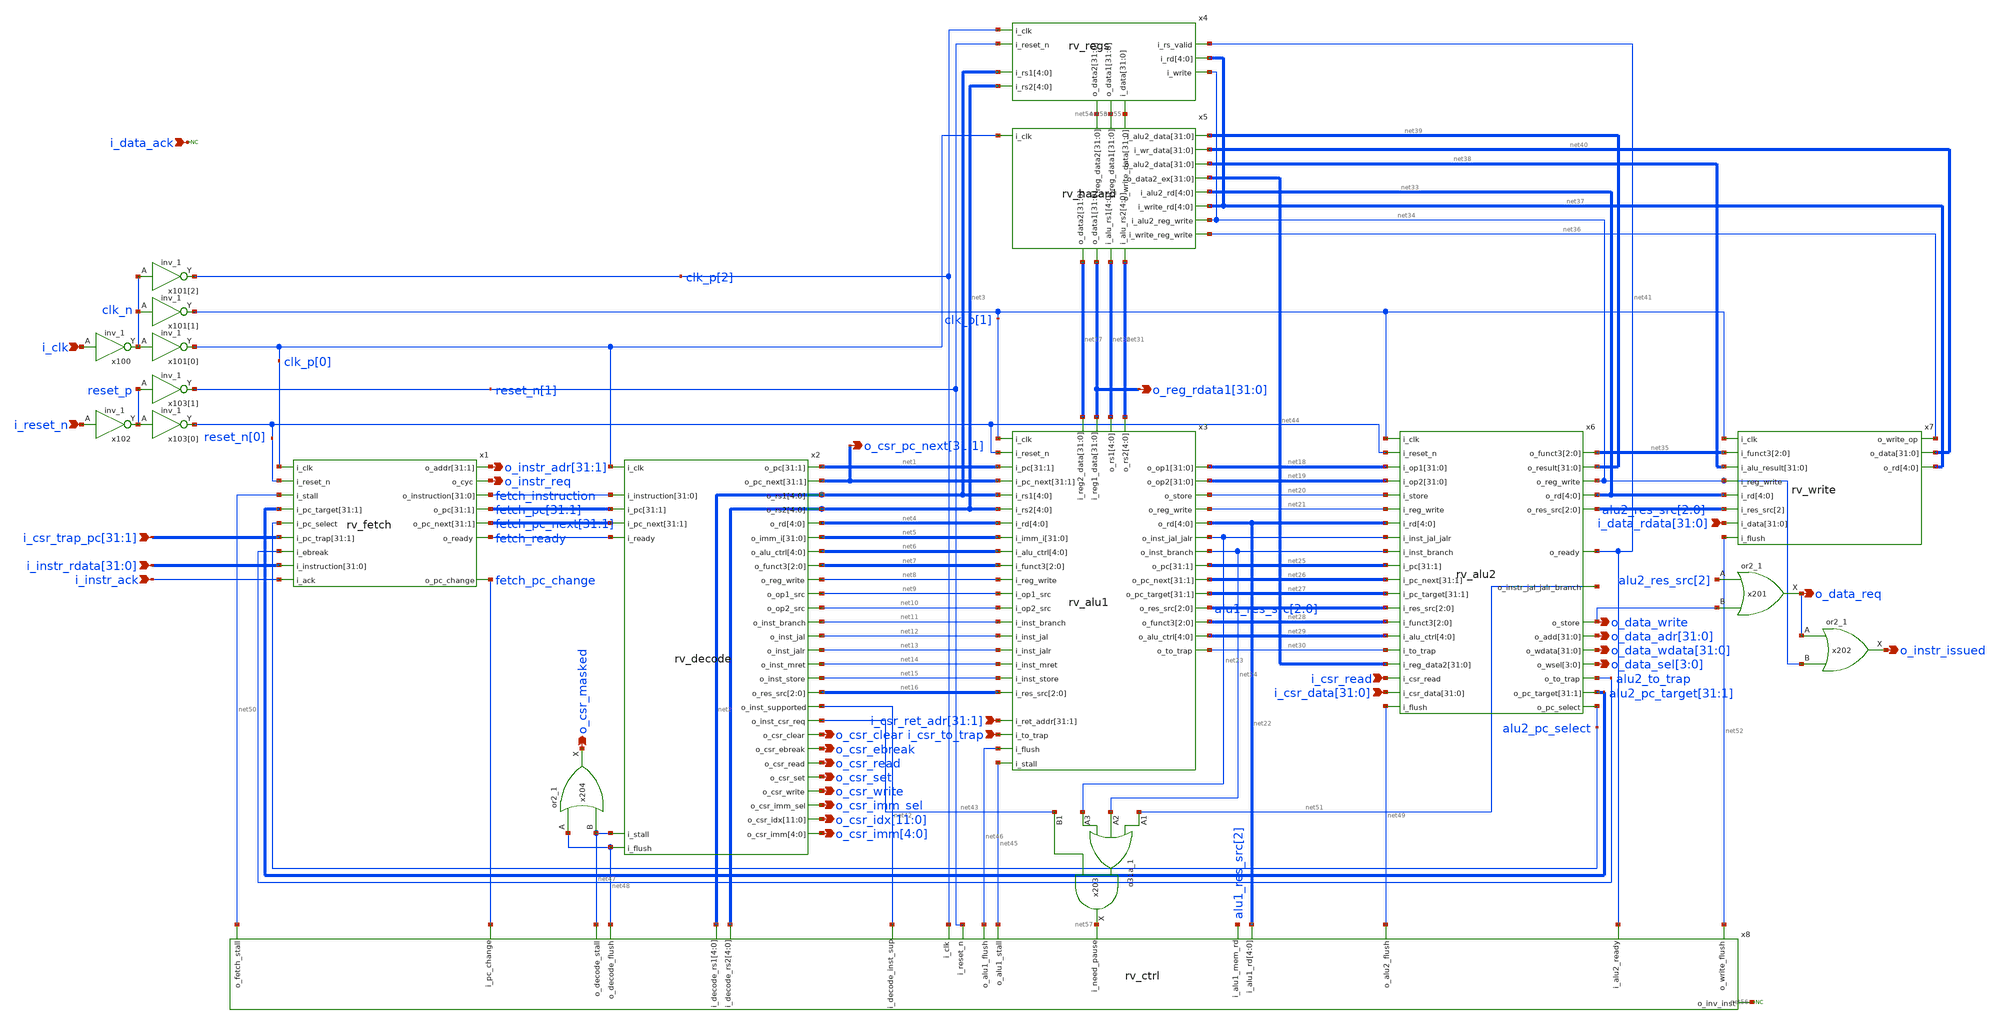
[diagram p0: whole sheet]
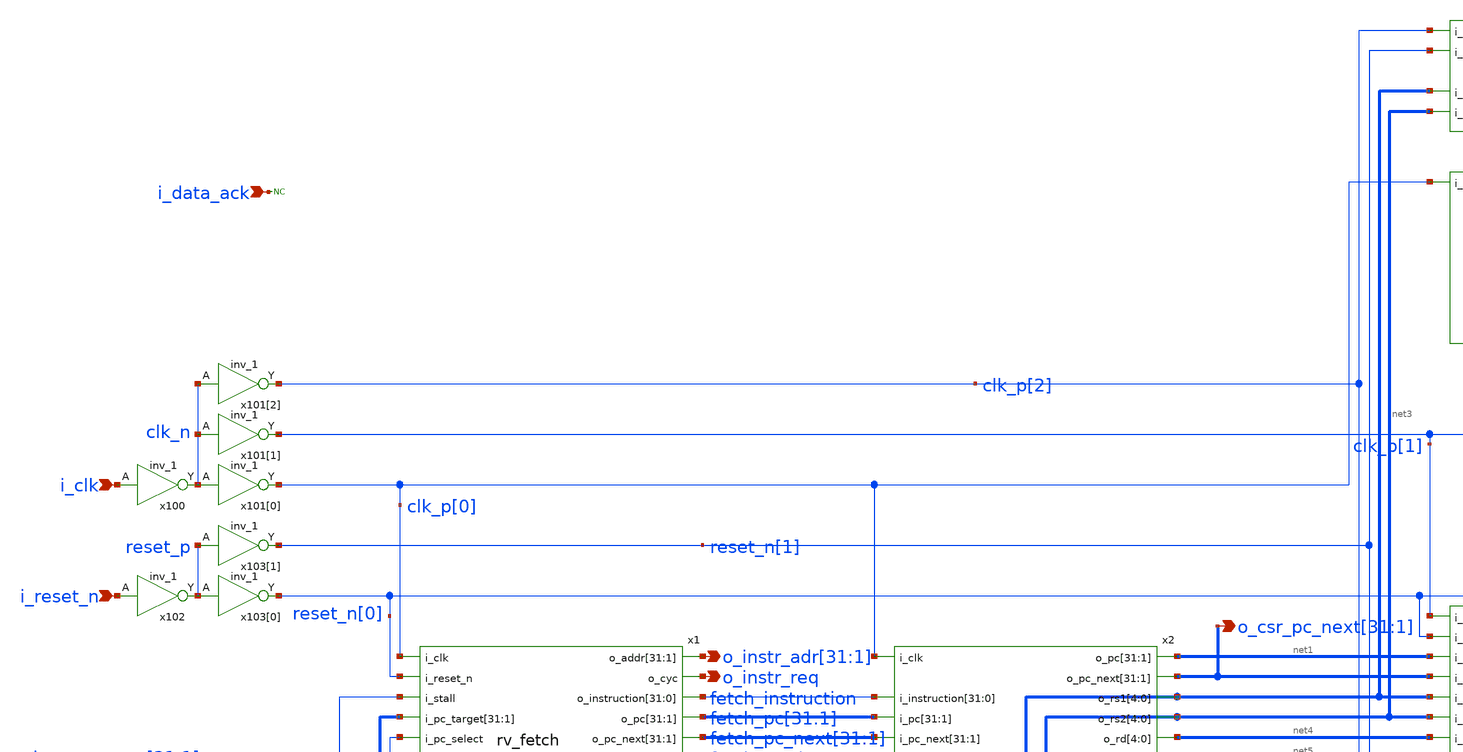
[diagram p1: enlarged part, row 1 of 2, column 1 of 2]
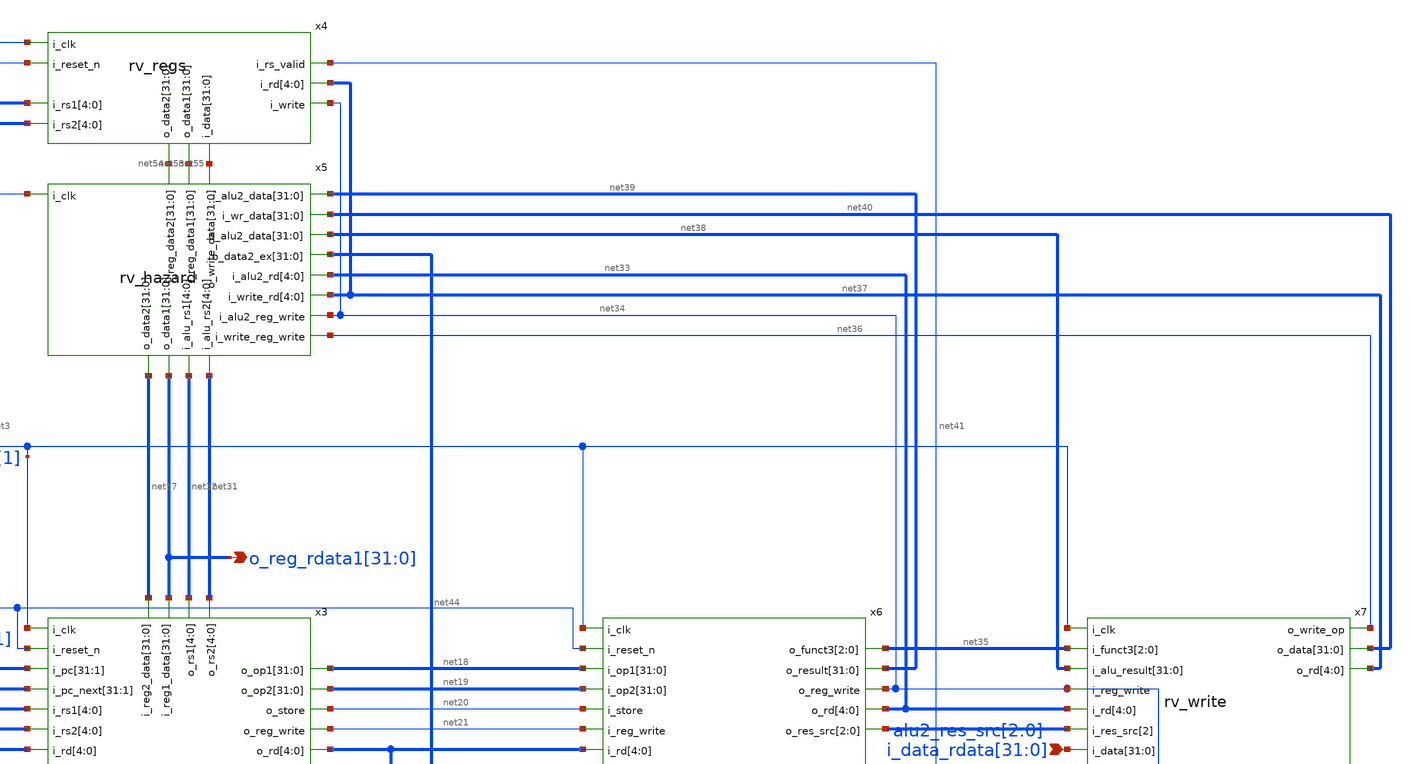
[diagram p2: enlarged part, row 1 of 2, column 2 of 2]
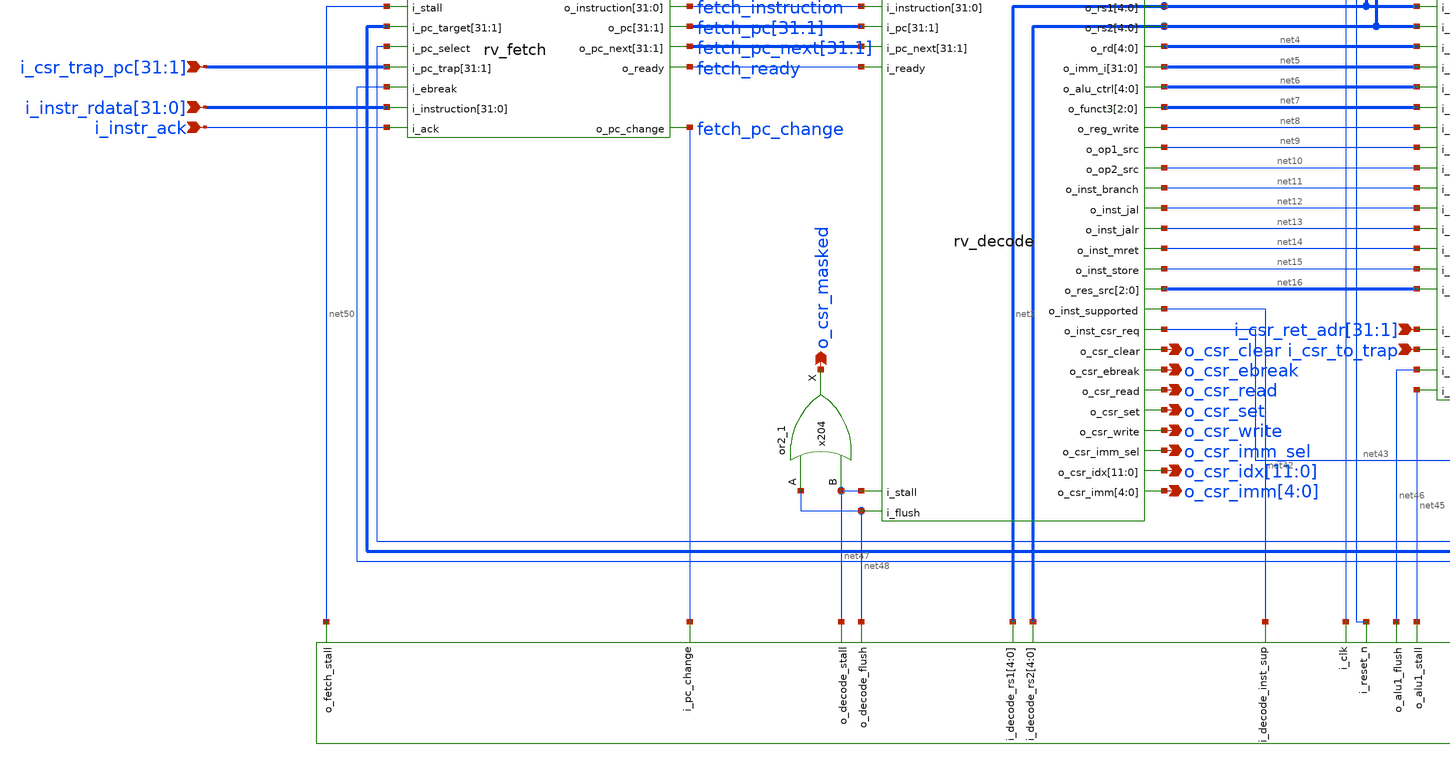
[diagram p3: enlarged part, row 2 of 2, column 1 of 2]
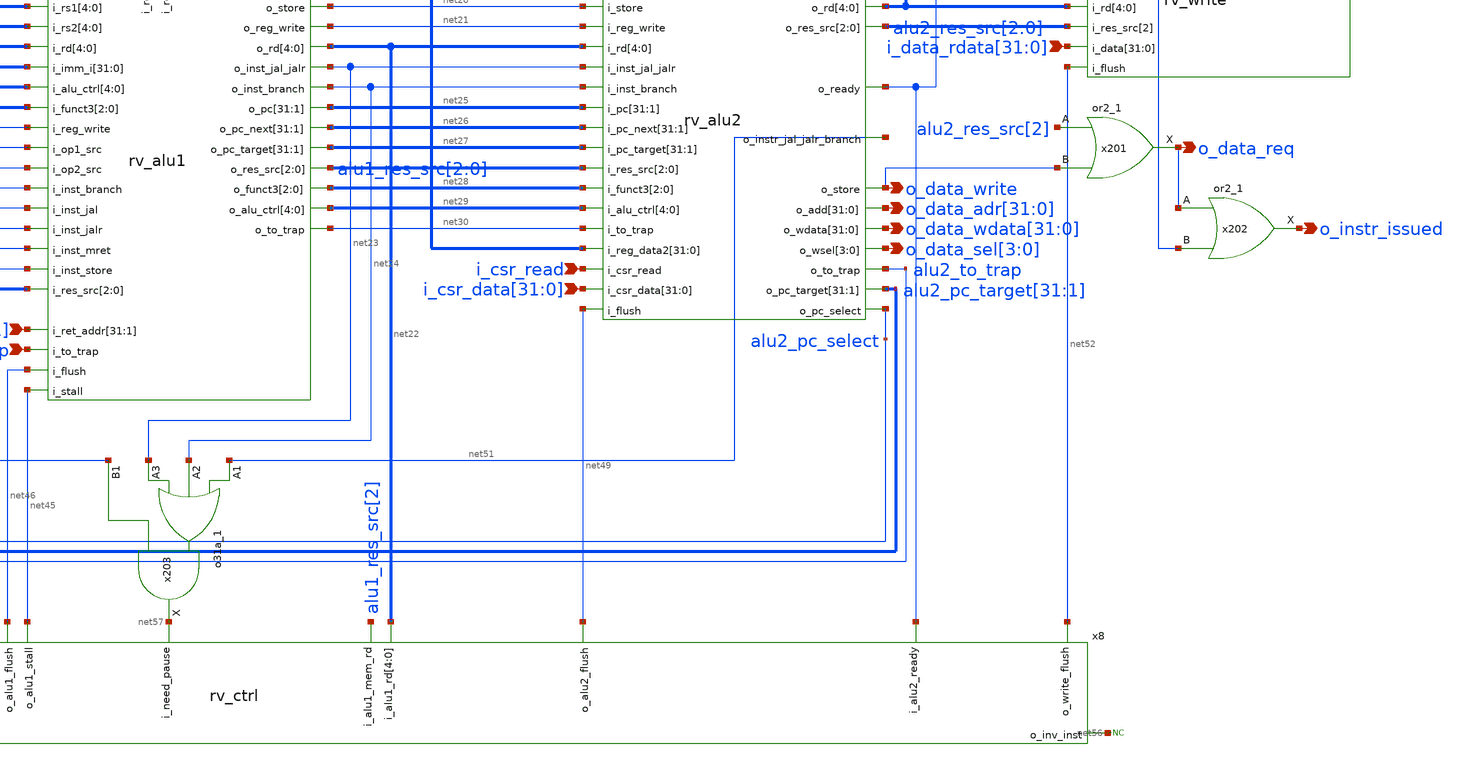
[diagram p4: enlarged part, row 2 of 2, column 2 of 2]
** sch_path: blocks/rv_core/rv_core.sch
**.subckt rv_core i_clk i_reset_n i_csr_read o_csr_clear o_data_req
*+ o_data_wdata[31],o_data_wdata[30],o_data_wdata[29],o_data_wdata[28],o_data_wdata[27],o_data_wdata[26],o_data_wdata[25],o_data_wdata[24],o_data_wdata[23],o_data_wdata[22],o_data_wdata[21],o_data_wdata[20],o_data_wdata[19],o_data_wdata[18],o_data_wdata[17],o_data_wdata[16],o_data_wdata[15],o_data_wdata[14],o_data_wdata[13],o_data_wdata[12],o_data_wdata[11],o_data_wdata[10],o_data_wdata[9],o_data_wdata[8],o_data_wdata[7],o_data_wdata[6],o_data_wdata[5],o_data_wdata[4],o_data_wdata[3],o_data_wdata[2],o_data_wdata[1],o_data_wdata[0] o_instr_issued
*+ o_data_adr[31],o_data_adr[30],o_data_adr[29],o_data_adr[28],o_data_adr[27],o_data_adr[26],o_data_adr[25],o_data_adr[24],o_data_adr[23],o_data_adr[22],o_data_adr[21],o_data_adr[20],o_data_adr[19],o_data_adr[18],o_data_adr[17],o_data_adr[16],o_data_adr[15],o_data_adr[14],o_data_adr[13],o_data_adr[12],o_data_adr[11],o_data_adr[10],o_data_adr[9],o_data_adr[8],o_data_adr[7],o_data_adr[6],o_data_adr[5],o_data_adr[4],o_data_adr[3],o_data_adr[2],o_data_adr[1],o_data_adr[0] o_data_sel[3],o_data_sel[2],o_data_sel[1],o_data_sel[0]
*+ i_csr_data[31],i_csr_data[30],i_csr_data[29],i_csr_data[28],i_csr_data[27],i_csr_data[26],i_csr_data[25],i_csr_data[24],i_csr_data[23],i_csr_data[22],i_csr_data[21],i_csr_data[20],i_csr_data[19],i_csr_data[18],i_csr_data[17],i_csr_data[16],i_csr_data[15],i_csr_data[14],i_csr_data[13],i_csr_data[12],i_csr_data[11],i_csr_data[10],i_csr_data[9],i_csr_data[8],i_csr_data[7],i_csr_data[6],i_csr_data[5],i_csr_data[4],i_csr_data[3],i_csr_data[2],i_csr_data[1],i_csr_data[0] i_csr_to_trap o_csr_ebreak o_csr_read o_csr_set o_csr_write o_csr_imm_sel
*+ i_csr_ret_adr[31],i_csr_ret_adr[30],i_csr_ret_adr[29],i_csr_ret_adr[28],i_csr_ret_adr[27],i_csr_ret_adr[26],i_csr_ret_adr[25],i_csr_ret_adr[24],i_csr_ret_adr[23],i_csr_ret_adr[22],i_csr_ret_adr[21],i_csr_ret_adr[20],i_csr_ret_adr[19],i_csr_ret_adr[18],i_csr_ret_adr[17],i_csr_ret_adr[16],i_csr_ret_adr[15],i_csr_ret_adr[14],i_csr_ret_adr[13],i_csr_ret_adr[12],i_csr_ret_adr[11],i_csr_ret_adr[10],i_csr_ret_adr[9],i_csr_ret_adr[8],i_csr_ret_adr[7],i_csr_ret_adr[6],i_csr_ret_adr[5],i_csr_ret_adr[4],i_csr_ret_adr[3],i_csr_ret_adr[2],i_csr_ret_adr[1]
*+ i_csr_trap_pc[31],i_csr_trap_pc[30],i_csr_trap_pc[29],i_csr_trap_pc[28],i_csr_trap_pc[27],i_csr_trap_pc[26],i_csr_trap_pc[25],i_csr_trap_pc[24],i_csr_trap_pc[23],i_csr_trap_pc[22],i_csr_trap_pc[21],i_csr_trap_pc[20],i_csr_trap_pc[19],i_csr_trap_pc[18],i_csr_trap_pc[17],i_csr_trap_pc[16],i_csr_trap_pc[15],i_csr_trap_pc[14],i_csr_trap_pc[13],i_csr_trap_pc[12],i_csr_trap_pc[11],i_csr_trap_pc[10],i_csr_trap_pc[9],i_csr_trap_pc[8],i_csr_trap_pc[7],i_csr_trap_pc[6],i_csr_trap_pc[5],i_csr_trap_pc[4],i_csr_trap_pc[3],i_csr_trap_pc[2],i_csr_trap_pc[1]
*+ o_csr_idx[11],o_csr_idx[10],o_csr_idx[9],o_csr_idx[8],o_csr_idx[7],o_csr_idx[6],o_csr_idx[5],o_csr_idx[4],o_csr_idx[3],o_csr_idx[2],o_csr_idx[1],o_csr_idx[0] o_csr_imm[4],o_csr_imm[3],o_csr_imm[2],o_csr_imm[1],o_csr_imm[0]
*+ o_csr_pc_next[31],o_csr_pc_next[30],o_csr_pc_next[29],o_csr_pc_next[28],o_csr_pc_next[27],o_csr_pc_next[26],o_csr_pc_next[25],o_csr_pc_next[24],o_csr_pc_next[23],o_csr_pc_next[22],o_csr_pc_next[21],o_csr_pc_next[20],o_csr_pc_next[19],o_csr_pc_next[18],o_csr_pc_next[17],o_csr_pc_next[16],o_csr_pc_next[15],o_csr_pc_next[14],o_csr_pc_next[13],o_csr_pc_next[12],o_csr_pc_next[11],o_csr_pc_next[10],o_csr_pc_next[9],o_csr_pc_next[8],o_csr_pc_next[7],o_csr_pc_next[6],o_csr_pc_next[5],o_csr_pc_next[4],o_csr_pc_next[3],o_csr_pc_next[2],o_csr_pc_next[1]
*+ o_reg_rdata1[31],o_reg_rdata1[30],o_reg_rdata1[29],o_reg_rdata1[28],o_reg_rdata1[27],o_reg_rdata1[26],o_reg_rdata1[25],o_reg_rdata1[24],o_reg_rdata1[23],o_reg_rdata1[22],o_reg_rdata1[21],o_reg_rdata1[20],o_reg_rdata1[19],o_reg_rdata1[18],o_reg_rdata1[17],o_reg_rdata1[16],o_reg_rdata1[15],o_reg_rdata1[14],o_reg_rdata1[13],o_reg_rdata1[12],o_reg_rdata1[11],o_reg_rdata1[10],o_reg_rdata1[9],o_reg_rdata1[8],o_reg_rdata1[7],o_reg_rdata1[6],o_reg_rdata1[5],o_reg_rdata1[4],o_reg_rdata1[3],o_reg_rdata1[2],o_reg_rdata1[1],o_reg_rdata1[0] i_data_ack o_data_write
*+ i_data_rdata[31],i_data_rdata[30],i_data_rdata[29],i_data_rdata[28],i_data_rdata[27],i_data_rdata[26],i_data_rdata[25],i_data_rdata[24],i_data_rdata[23],i_data_rdata[22],i_data_rdata[21],i_data_rdata[20],i_data_rdata[19],i_data_rdata[18],i_data_rdata[17],i_data_rdata[16],i_data_rdata[15],i_data_rdata[14],i_data_rdata[13],i_data_rdata[12],i_data_rdata[11],i_data_rdata[10],i_data_rdata[9],i_data_rdata[8],i_data_rdata[7],i_data_rdata[6],i_data_rdata[5],i_data_rdata[4],i_data_rdata[3],i_data_rdata[2],i_data_rdata[1],i_data_rdata[0] i_instr_ack o_instr_req
*+ i_instr_rdata[31],i_instr_rdata[30],i_instr_rdata[29],i_instr_rdata[28],i_instr_rdata[27],i_instr_rdata[26],i_instr_rdata[25],i_instr_rdata[24],i_instr_rdata[23],i_instr_rdata[22],i_instr_rdata[21],i_instr_rdata[20],i_instr_rdata[19],i_instr_rdata[18],i_instr_rdata[17],i_instr_rdata[16],i_instr_rdata[15],i_instr_rdata[14],i_instr_rdata[13],i_instr_rdata[12],i_instr_rdata[11],i_instr_rdata[10],i_instr_rdata[9],i_instr_rdata[8],i_instr_rdata[7],i_instr_rdata[6],i_instr_rdata[5],i_instr_rdata[4],i_instr_rdata[3],i_instr_rdata[2],i_instr_rdata[1],i_instr_rdata[0]
*+ o_instr_adr[31],o_instr_adr[30],o_instr_adr[29],o_instr_adr[28],o_instr_adr[27],o_instr_adr[26],o_instr_adr[25],o_instr_adr[24],o_instr_adr[23],o_instr_adr[22],o_instr_adr[21],o_instr_adr[20],o_instr_adr[19],o_instr_adr[18],o_instr_adr[17],o_instr_adr[16],o_instr_adr[15],o_instr_adr[14],o_instr_adr[13],o_instr_adr[12],o_instr_adr[11],o_instr_adr[10],o_instr_adr[9],o_instr_adr[8],o_instr_adr[7],o_instr_adr[6],o_instr_adr[5],o_instr_adr[4],o_instr_adr[3],o_instr_adr[2],o_instr_adr[1] o_csr_masked
*.ipin i_clk
*.ipin i_reset_n
*.ipin i_csr_read
*.opin o_csr_clear
*.opin o_data_req
*.opin
*+ o_data_wdata[31],o_data_wdata[30],o_data_wdata[29],o_data_wdata[28],o_data_wdata[27],o_data_wdata[26],o_data_wdata[25],o_data_wdata[24],o_data_wdata[23],o_data_wdata[22],o_data_wdata[21],o_data_wdata[20],o_data_wdata[19],o_data_wdata[18],o_data_wdata[17],o_data_wdata[16],o_data_wdata[15],o_data_wdata[14],o_data_wdata[13],o_data_wdata[12],o_data_wdata[11],o_data_wdata[10],o_data_wdata[9],o_data_wdata[8],o_data_wdata[7],o_data_wdata[6],o_data_wdata[5],o_data_wdata[4],o_data_wdata[3],o_data_wdata[2],o_data_wdata[1],o_data_wdata[0]
*.opin o_instr_issued
*.opin
*+ o_data_adr[31],o_data_adr[30],o_data_adr[29],o_data_adr[28],o_data_adr[27],o_data_adr[26],o_data_adr[25],o_data_adr[24],o_data_adr[23],o_data_adr[22],o_data_adr[21],o_data_adr[20],o_data_adr[19],o_data_adr[18],o_data_adr[17],o_data_adr[16],o_data_adr[15],o_data_adr[14],o_data_adr[13],o_data_adr[12],o_data_adr[11],o_data_adr[10],o_data_adr[9],o_data_adr[8],o_data_adr[7],o_data_adr[6],o_data_adr[5],o_data_adr[4],o_data_adr[3],o_data_adr[2],o_data_adr[1],o_data_adr[0]
*.opin o_data_sel[3],o_data_sel[2],o_data_sel[1],o_data_sel[0]
*.ipin
*+ i_csr_data[31],i_csr_data[30],i_csr_data[29],i_csr_data[28],i_csr_data[27],i_csr_data[26],i_csr_data[25],i_csr_data[24],i_csr_data[23],i_csr_data[22],i_csr_data[21],i_csr_data[20],i_csr_data[19],i_csr_data[18],i_csr_data[17],i_csr_data[16],i_csr_data[15],i_csr_data[14],i_csr_data[13],i_csr_data[12],i_csr_data[11],i_csr_data[10],i_csr_data[9],i_csr_data[8],i_csr_data[7],i_csr_data[6],i_csr_data[5],i_csr_data[4],i_csr_data[3],i_csr_data[2],i_csr_data[1],i_csr_data[0]
*.ipin i_csr_to_trap
*.opin o_csr_ebreak
*.opin o_csr_read
*.opin o_csr_set
*.opin o_csr_write
*.opin o_csr_imm_sel
*.ipin
*+ i_csr_ret_adr[31],i_csr_ret_adr[30],i_csr_ret_adr[29],i_csr_ret_adr[28],i_csr_ret_adr[27],i_csr_ret_adr[26],i_csr_ret_adr[25],i_csr_ret_adr[24],i_csr_ret_adr[23],i_csr_ret_adr[22],i_csr_ret_adr[21],i_csr_ret_adr[20],i_csr_ret_adr[19],i_csr_ret_adr[18],i_csr_ret_adr[17],i_csr_ret_adr[16],i_csr_ret_adr[15],i_csr_ret_adr[14],i_csr_ret_adr[13],i_csr_ret_adr[12],i_csr_ret_adr[11],i_csr_ret_adr[10],i_csr_ret_adr[9],i_csr_ret_adr[8],i_csr_ret_adr[7],i_csr_ret_adr[6],i_csr_ret_adr[5],i_csr_ret_adr[4],i_csr_ret_adr[3],i_csr_ret_adr[2],i_csr_ret_adr[1]
*.ipin
*+ i_csr_trap_pc[31],i_csr_trap_pc[30],i_csr_trap_pc[29],i_csr_trap_pc[28],i_csr_trap_pc[27],i_csr_trap_pc[26],i_csr_trap_pc[25],i_csr_trap_pc[24],i_csr_trap_pc[23],i_csr_trap_pc[22],i_csr_trap_pc[21],i_csr_trap_pc[20],i_csr_trap_pc[19],i_csr_trap_pc[18],i_csr_trap_pc[17],i_csr_trap_pc[16],i_csr_trap_pc[15],i_csr_trap_pc[14],i_csr_trap_pc[13],i_csr_trap_pc[12],i_csr_trap_pc[11],i_csr_trap_pc[10],i_csr_trap_pc[9],i_csr_trap_pc[8],i_csr_trap_pc[7],i_csr_trap_pc[6],i_csr_trap_pc[5],i_csr_trap_pc[4],i_csr_trap_pc[3],i_csr_trap_pc[2],i_csr_trap_pc[1]
*.opin
*+ o_csr_idx[11],o_csr_idx[10],o_csr_idx[9],o_csr_idx[8],o_csr_idx[7],o_csr_idx[6],o_csr_idx[5],o_csr_idx[4],o_csr_idx[3],o_csr_idx[2],o_csr_idx[1],o_csr_idx[0]
*.opin o_csr_imm[4],o_csr_imm[3],o_csr_imm[2],o_csr_imm[1],o_csr_imm[0]
*.opin
*+ o_csr_pc_next[31],o_csr_pc_next[30],o_csr_pc_next[29],o_csr_pc_next[28],o_csr_pc_next[27],o_csr_pc_next[26],o_csr_pc_next[25],o_csr_pc_next[24],o_csr_pc_next[23],o_csr_pc_next[22],o_csr_pc_next[21],o_csr_pc_next[20],o_csr_pc_next[19],o_csr_pc_next[18],o_csr_pc_next[17],o_csr_pc_next[16],o_csr_pc_next[15],o_csr_pc_next[14],o_csr_pc_next[13],o_csr_pc_next[12],o_csr_pc_next[11],o_csr_pc_next[10],o_csr_pc_next[9],o_csr_pc_next[8],o_csr_pc_next[7],o_csr_pc_next[6],o_csr_pc_next[5],o_csr_pc_next[4],o_csr_pc_next[3],o_csr_pc_next[2],o_csr_pc_next[1]
*.opin
*+ o_reg_rdata1[31],o_reg_rdata1[30],o_reg_rdata1[29],o_reg_rdata1[28],o_reg_rdata1[27],o_reg_rdata1[26],o_reg_rdata1[25],o_reg_rdata1[24],o_reg_rdata1[23],o_reg_rdata1[22],o_reg_rdata1[21],o_reg_rdata1[20],o_reg_rdata1[19],o_reg_rdata1[18],o_reg_rdata1[17],o_reg_rdata1[16],o_reg_rdata1[15],o_reg_rdata1[14],o_reg_rdata1[13],o_reg_rdata1[12],o_reg_rdata1[11],o_reg_rdata1[10],o_reg_rdata1[9],o_reg_rdata1[8],o_reg_rdata1[7],o_reg_rdata1[6],o_reg_rdata1[5],o_reg_rdata1[4],o_reg_rdata1[3],o_reg_rdata1[2],o_reg_rdata1[1],o_reg_rdata1[0]
*.ipin i_data_ack
*.opin o_data_write
*.ipin
*+ i_data_rdata[31],i_data_rdata[30],i_data_rdata[29],i_data_rdata[28],i_data_rdata[27],i_data_rdata[26],i_data_rdata[25],i_data_rdata[24],i_data_rdata[23],i_data_rdata[22],i_data_rdata[21],i_data_rdata[20],i_data_rdata[19],i_data_rdata[18],i_data_rdata[17],i_data_rdata[16],i_data_rdata[15],i_data_rdata[14],i_data_rdata[13],i_data_rdata[12],i_data_rdata[11],i_data_rdata[10],i_data_rdata[9],i_data_rdata[8],i_data_rdata[7],i_data_rdata[6],i_data_rdata[5],i_data_rdata[4],i_data_rdata[3],i_data_rdata[2],i_data_rdata[1],i_data_rdata[0]
*.ipin i_instr_ack
*.opin o_instr_req
*.ipin
*+ i_instr_rdata[31],i_instr_rdata[30],i_instr_rdata[29],i_instr_rdata[28],i_instr_rdata[27],i_instr_rdata[26],i_instr_rdata[25],i_instr_rdata[24],i_instr_rdata[23],i_instr_rdata[22],i_instr_rdata[21],i_instr_rdata[20],i_instr_rdata[19],i_instr_rdata[18],i_instr_rdata[17],i_instr_rdata[16],i_instr_rdata[15],i_instr_rdata[14],i_instr_rdata[13],i_instr_rdata[12],i_instr_rdata[11],i_instr_rdata[10],i_instr_rdata[9],i_instr_rdata[8],i_instr_rdata[7],i_instr_rdata[6],i_instr_rdata[5],i_instr_rdata[4],i_instr_rdata[3],i_instr_rdata[2],i_instr_rdata[1],i_instr_rdata[0]
*.opin
*+ o_instr_adr[31],o_instr_adr[30],o_instr_adr[29],o_instr_adr[28],o_instr_adr[27],o_instr_adr[26],o_instr_adr[25],o_instr_adr[24],o_instr_adr[23],o_instr_adr[22],o_instr_adr[21],o_instr_adr[20],o_instr_adr[19],o_instr_adr[18],o_instr_adr[17],o_instr_adr[16],o_instr_adr[15],o_instr_adr[14],o_instr_adr[13],o_instr_adr[12],o_instr_adr[11],o_instr_adr[10],o_instr_adr[9],o_instr_adr[8],o_instr_adr[7],o_instr_adr[6],o_instr_adr[5],o_instr_adr[4],o_instr_adr[3],o_instr_adr[2],o_instr_adr[1]
*.opin o_csr_masked
x1 fetch_pc_change clk_p[0] reset_n[0] o_instr_adr[31] o_instr_adr[30] o_instr_adr[29]
+ o_instr_adr[28] o_instr_adr[27] o_instr_adr[26] o_instr_adr[25] o_instr_adr[24] o_instr_adr[23] o_instr_adr[22]
+ o_instr_adr[21] o_instr_adr[20] o_instr_adr[19] o_instr_adr[18] o_instr_adr[17] o_instr_adr[16] o_instr_adr[15]
+ o_instr_adr[14] o_instr_adr[13] o_instr_adr[12] o_instr_adr[11] o_instr_adr[10] o_instr_adr[9] o_instr_adr[8]
+ o_instr_adr[7] o_instr_adr[6] o_instr_adr[5] o_instr_adr[4] o_instr_adr[3] o_instr_adr[2] o_instr_adr[1]
+ o_instr_req net50 fetch_instruction fetch_instruction fetch_instruction fetch_instruction fetch_instruction
+ fetch_instruction fetch_instruction fetch_instruction fetch_instruction fetch_instruction fetch_instruction
+ fetch_instruction fetch_instruction fetch_instruction fetch_instruction fetch_instruction fetch_instruction
+ fetch_instruction fetch_instruction fetch_instruction fetch_instruction fetch_instruction fetch_instruction
+ fetch_instruction fetch_instruction fetch_instruction fetch_instruction fetch_instruction fetch_instruction
+ fetch_instruction fetch_instruction fetch_instruction alu2_pc_target[31] alu2_pc_target[30] alu2_pc_target[29]
+ alu2_pc_target[28] alu2_pc_target[27] alu2_pc_target[26] alu2_pc_target[25] alu2_pc_target[24] alu2_pc_target[23]
+ alu2_pc_target[22] alu2_pc_target[21] alu2_pc_target[20] alu2_pc_target[19] alu2_pc_target[18] alu2_pc_target[17]
+ alu2_pc_target[16] alu2_pc_target[15] alu2_pc_target[14] alu2_pc_target[13] alu2_pc_target[12] alu2_pc_target[11]
+ alu2_pc_target[10] alu2_pc_target[9] alu2_pc_target[8] alu2_pc_target[7] alu2_pc_target[6] alu2_pc_target[5]
+ alu2_pc_target[4] alu2_pc_target[3] alu2_pc_target[2] alu2_pc_target[1] alu2_pc_select fetch_pc[31] fetch_pc[30]
+ fetch_pc[29] fetch_pc[28] fetch_pc[27] fetch_pc[26] fetch_pc[25] fetch_pc[24] fetch_pc[23] fetch_pc[22]
+ fetch_pc[21] fetch_pc[20] fetch_pc[19] fetch_pc[18] fetch_pc[17] fetch_pc[16] fetch_pc[15] fetch_pc[14]
+ fetch_pc[13] fetch_pc[12] fetch_pc[11] fetch_pc[10] fetch_pc[9] fetch_pc[8] fetch_pc[7] fetch_pc[6] fetch_pc[5]
+ fetch_pc[4] fetch_pc[3] fetch_pc[2] fetch_pc[1] fetch_pc_next[31] fetch_pc_next[30] fetch_pc_next[29]
+ fetch_pc_next[28] fetch_pc_next[27] fetch_pc_next[26] fetch_pc_next[25] fetch_pc_next[24] fetch_pc_next[23]
+ fetch_pc_next[22] fetch_pc_next[21] fetch_pc_next[20] fetch_pc_next[19] fetch_pc_next[18] fetch_pc_next[17]
+ fetch_pc_next[16] fetch_pc_next[15] fetch_pc_next[14] fetch_pc_next[13] fetch_pc_next[12] fetch_pc_next[11]
+ fetch_pc_next[10] fetch_pc_next[9] fetch_pc_next[8] fetch_pc_next[7] fetch_pc_next[6] fetch_pc_next[5]
+ fetch_pc_next[4] fetch_pc_next[3] fetch_pc_next[2] fetch_pc_next[1] i_csr_trap_pc[31] i_csr_trap_pc[30]
+ i_csr_trap_pc[29] i_csr_trap_pc[28] i_csr_trap_pc[27] i_csr_trap_pc[26] i_csr_trap_pc[25] i_csr_trap_pc[24]
+ i_csr_trap_pc[23] i_csr_trap_pc[22] i_csr_trap_pc[21] i_csr_trap_pc[20] i_csr_trap_pc[19] i_csr_trap_pc[18]
+ i_csr_trap_pc[17] i_csr_trap_pc[16] i_csr_trap_pc[15] i_csr_trap_pc[14] i_csr_trap_pc[13] i_csr_trap_pc[12]
+ i_csr_trap_pc[11] i_csr_trap_pc[10] i_csr_trap_pc[9] i_csr_trap_pc[8] i_csr_trap_pc[7] i_csr_trap_pc[6]
+ i_csr_trap_pc[5] i_csr_trap_pc[4] i_csr_trap_pc[3] i_csr_trap_pc[2] i_csr_trap_pc[1] fetch_ready alu2_to_trap
+ i_instr_rdata[31] i_instr_rdata[30] i_instr_rdata[29] i_instr_rdata[28] i_instr_rdata[27] i_instr_rdata[26]
+ i_instr_rdata[25] i_instr_rdata[24] i_instr_rdata[23] i_instr_rdata[22] i_instr_rdata[21] i_instr_rdata[20]
+ i_instr_rdata[19] i_instr_rdata[18] i_instr_rdata[17] i_instr_rdata[16] i_instr_rdata[15] i_instr_rdata[14]
+ i_instr_rdata[13] i_instr_rdata[12] i_instr_rdata[11] i_instr_rdata[10] i_instr_rdata[9] i_instr_rdata[8]
+ i_instr_rdata[7] i_instr_rdata[6] i_instr_rdata[5] i_instr_rdata[4] i_instr_rdata[3] i_instr_rdata[2]
+ i_instr_rdata[1] i_instr_rdata[0] i_instr_ack rv_fetch
x100 i_clk VSS VSS VCC VCC clk_n sky130_fd_sc_hd__inv_1
x102 i_reset_n VSS VSS VCC VCC reset_p sky130_fd_sc_hd__inv_1
x103[0] reset_p VSS VSS VCC VCC reset_n[0] sky130_fd_sc_hd__inv_1
x101[2] clk_n VSS VSS VCC VCC clk_p[2] sky130_fd_sc_hd__inv_1
x101[1] clk_n VSS VSS VCC VCC clk_p[1] sky130_fd_sc_hd__inv_1
x101[0] clk_n VSS VSS VCC VCC clk_p[0] sky130_fd_sc_hd__inv_1
x103[1] reset_p VSS VSS VCC VCC reset_n[1] sky130_fd_sc_hd__inv_1
x2 net1[30] net1[29] net1[28] net1[27] net1[26] net1[25] net1[24] net1[23] net1[22] net1[21]
+ net1[20] net1[19] net1[18] net1[17] net1[16] net1[15] net1[14] net1[13] net1[12] net1[11] net1[10] net1[9]
+ net1[8] net1[7] net1[6] net1[5] net1[4] net1[3] net1[2] net1[1] net1[0] clk_p[0] net47 o_csr_pc_next[31]
+ o_csr_pc_next[30] o_csr_pc_next[29] o_csr_pc_next[28] o_csr_pc_next[27] o_csr_pc_next[26] o_csr_pc_next[25]
+ o_csr_pc_next[24] o_csr_pc_next[23] o_csr_pc_next[22] o_csr_pc_next[21] o_csr_pc_next[20] o_csr_pc_next[19]
+ o_csr_pc_next[18] o_csr_pc_next[17] o_csr_pc_next[16] o_csr_pc_next[15] o_csr_pc_next[14] o_csr_pc_next[13]
+ o_csr_pc_next[12] o_csr_pc_next[11] o_csr_pc_next[10] o_csr_pc_next[9] o_csr_pc_next[8] o_csr_pc_next[7]
+ o_csr_pc_next[6] o_csr_pc_next[5] o_csr_pc_next[4] o_csr_pc_next[3] o_csr_pc_next[2] o_csr_pc_next[1] net48 net2[4]
+ net2[3] net2[2] net2[1] net2[0] fetch_instruction fetch_instruction fetch_instruction fetch_instruction
+ fetch_instruction fetch_instruction fetch_instruction fetch_instruction fetch_instruction fetch_instruction
+ fetch_instruction fetch_instruction fetch_instruction fetch_instruction fetch_instruction fetch_instruction
+ fetch_instruction fetch_instruction fetch_instruction fetch_instruction fetch_instruction fetch_instruction
+ fetch_instruction fetch_instruction fetch_instruction fetch_instruction fetch_instruction fetch_instruction
+ fetch_instruction fetch_instruction fetch_instruction fetch_instruction net3[4] net3[3] net3[2] net3[1] net3[0]
+ net4[4] net4[3] net4[2] net4[1] net4[0] fetch_pc[31] fetch_pc[30] fetch_pc[29] fetch_pc[28] fetch_pc[27]
+ fetch_pc[26] fetch_pc[25] fetch_pc[24] fetch_pc[23] fetch_pc[22] fetch_pc[21] fetch_pc[20] fetch_pc[19]
+ fetch_pc[18] fetch_pc[17] fetch_pc[16] fetch_pc[15] fetch_pc[14] fetch_pc[13] fetch_pc[12] fetch_pc[11]
+ fetch_pc[10] fetch_pc[9] fetch_pc[8] fetch_pc[7] fetch_pc[6] fetch_pc[5] fetch_pc[4] fetch_pc[3] fetch_pc[2]
+ fetch_pc[1] net5[31] net5[30] net5[29] net5[28] net5[27] net5[26] net5[25] net5[24] net5[23] net5[22] net5[21]
+ net5[20] net5[19] net5[18] net5[17] net5[16] net5[15] net5[14] net5[13] net5[12] net5[11] net5[10] net5[9]
+ net5[8] net5[7] net5[6] net5[5] net5[4] net5[3] net5[2] net5[1] net5[0] fetch_pc_next[31] fetch_pc_next[30]
+ fetch_pc_next[29] fetch_pc_next[28] fetch_pc_next[27] fetch_pc_next[26] fetch_pc_next[25] fetch_pc_next[24]
+ fetch_pc_next[23] fetch_pc_next[22] fetch_pc_next[21] fetch_pc_next[20] fetch_pc_next[19] fetch_pc_next[18]
+ fetch_pc_next[17] fetch_pc_next[16] fetch_pc_next[15] fetch_pc_next[14] fetch_pc_next[13] fetch_pc_next[12]
+ fetch_pc_next[11] fetch_pc_next[10] fetch_pc_next[9] fetch_pc_next[8] fetch_pc_next[7] fetch_pc_next[6]
+ fetch_pc_next[5] fetch_pc_next[4] fetch_pc_next[3] fetch_pc_next[2] fetch_pc_next[1] fetch_ready net6[4] net6[3]
+ net6[2] net6[1] net6[0] net7[2] net7[1] net7[0] net8 net9 net10 net11 net43 net12 net13 net14 net15 net42
+ net16[2] net16[1] net16[0] o_csr_clear o_csr_ebreak o_csr_read o_csr_set o_csr_write o_csr_imm_sel
+ o_csr_idx[11] o_csr_idx[10] o_csr_idx[9] o_csr_idx[8] o_csr_idx[7] o_csr_idx[6] o_csr_idx[5] o_csr_idx[4]
+ o_csr_idx[3] o_csr_idx[2] o_csr_idx[1] o_csr_idx[0] o_csr_imm[4] o_csr_imm[3] o_csr_imm[2] o_csr_imm[1]
+ o_csr_imm[0] rv_decode
x3 clk_p[1] net18[31] net18[30] net18[29] net18[28] net18[27] net18[26] net18[25] net18[24]
+ net18[23] net18[22] net18[21] net18[20] net18[19] net18[18] net18[17] net18[16] net18[15] net18[14] net18[13]
+ net18[12] net18[11] net18[10] net18[9] net18[8] net18[7] net18[6] net18[5] net18[4] net18[3] net18[2]
+ net18[1] net18[0] reset_n[0] net19[31] net19[30] net19[29] net19[28] net19[27] net19[26] net19[25] net19[24]
+ net19[23] net19[22] net19[21] net19[20] net19[19] net19[18] net19[17] net19[16] net19[15] net19[14] net19[13]
+ net19[12] net19[11] net19[10] net19[9] net19[8] net19[7] net19[6] net19[5] net19[4] net19[3] net19[2]
+ net19[1] net19[0] net1[30] net1[29] net1[28] net1[27] net1[26] net1[25] net1[24] net1[23] net1[22] net1[21]
+ net1[20] net1[19] net1[18] net1[17] net1[16] net1[15] net1[14] net1[13] net1[12] net1[11] net1[10] net1[9]
+ net1[8] net1[7] net1[6] net1[5] net1[4] net1[3] net1[2] net1[1] net1[0] net20 net21 o_csr_pc_next[31]
+ o_csr_pc_next[30] o_csr_pc_next[29] o_csr_pc_next[28] o_csr_pc_next[27] o_csr_pc_next[26] o_csr_pc_next[25]
+ o_csr_pc_next[24] o_csr_pc_next[23] o_csr_pc_next[22] o_csr_pc_next[21] o_csr_pc_next[20] o_csr_pc_next[19]
+ o_csr_pc_next[18] o_csr_pc_next[17] o_csr_pc_next[16] o_csr_pc_next[15] o_csr_pc_next[14] o_csr_pc_next[13]
+ o_csr_pc_next[12] o_csr_pc_next[11] o_csr_pc_next[10] o_csr_pc_next[9] o_csr_pc_next[8] o_csr_pc_next[7]
+ o_csr_pc_next[6] o_csr_pc_next[5] o_csr_pc_next[4] o_csr_pc_next[3] o_csr_pc_next[2] o_csr_pc_next[1] net32[4]
+ net32[3] net32[2] net32[1] net32[0] net2[4] net2[3] net2[2] net2[1] net2[0] net3[4] net3[3] net3[2] net3[1]
+ net3[0] net31[4] net31[3] net31[2] net31[1] net31[0] net4[4] net4[3] net4[2] net4[1] net4[0] net22[4]
+ net22[3] net22[2] net22[1] net22[0] net5[31] net5[30] net5[29] net5[28] net5[27] net5[26] net5[25] net5[24]
+ net5[23] net5[22] net5[21] net5[20] net5[19] net5[18] net5[17] net5[16] net5[15] net5[14] net5[13] net5[12]
+ net5[11] net5[10] net5[9] net5[8] net5[7] net5[6] net5[5] net5[4] net5[3] net5[2] net5[1] net5[0] net23
+ net6[4] net6[3] net6[2] net6[1] net6[0] net24 net7[2] net7[1] net7[0] net25[30] net25[29] net25[28]
+ net25[27] net25[26] net25[25] net25[24] net25[23] net25[22] net25[21] net25[20] net25[19] net25[18] net25[17]
+ net25[16] net25[15] net25[14] net25[13] net25[12] net25[11] net25[10] net25[9] net25[8] net25[7] net25[6]
+ net25[5] net25[4] net25[3] net25[2] net25[1] net25[0] net26[30] net26[29] net26[28] net26[27] net26[26]
+ net26[25] net26[24] net26[23] net26[22] net26[21] net26[20] net26[19] net26[18] net26[17] net26[16] net26[15]
+ net26[14] net26[13] net26[12] net26[11] net26[10] net26[9] net26[8] net26[7] net26[6] net26[5] net26[4]
+ net26[3] net26[2] net26[1] net26[0] net8 net27[30] net27[29] net27[28] net27[27] net27[26] net27[25]
+ net27[24] net27[23] net27[22] net27[21] net27[20] net27[19] net27[18] net27[17] net27[16] net27[15] net27[14]
+ net27[13] net27[12] net27[11] net27[10] net27[9] net27[8] net27[7] net27[6] net27[5] net27[4] net27[3]
+ net27[2] net27[1] net27[0] net9 net10 alu1_res_src[2] alu1_res_src[1] alu1_res_src[0] net11 net28[2]
+ net28[1] net28[0] net29[4] net29[3] net29[2] net29[1] net29[0] net12 net30 net13 net14 net15 net16[2]
+ net16[1] net16[0] o_reg_rdata1[31] o_reg_rdata1[30] o_reg_rdata1[29] o_reg_rdata1[28] o_reg_rdata1[27]
+ o_reg_rdata1[26] o_reg_rdata1[25] o_reg_rdata1[24] o_reg_rdata1[23] o_reg_rdata1[22] o_reg_rdata1[21]
+ o_reg_rdata1[20] o_reg_rdata1[19] o_reg_rdata1[18] o_reg_rdata1[17] o_reg_rdata1[16] o_reg_rdata1[15]
+ o_reg_rdata1[14] o_reg_rdata1[13] o_reg_rdata1[12] o_reg_rdata1[11] o_reg_rdata1[10] o_reg_rdata1[9] o_reg_rdata1[8]
+ o_reg_rdata1[7] o_reg_rdata1[6] o_reg_rdata1[5] o_reg_rdata1[4] o_reg_rdata1[3] o_reg_rdata1[2] o_reg_rdata1[1]
+ o_reg_rdata1[0] net17[31] net17[30] net17[29] net17[28] net17[27] net17[26] net17[25] net17[24] net17[23] net17[22]
+ net17[21] net17[20] net17[19] net17[18] net17[17] net17[16] net17[15] net17[14] net17[13] net17[12] net17[11]
+ net17[10] net17[9] net17[8] net17[7] net17[6] net17[5] net17[4] net17[3] net17[2] net17[1] net17[0]
+ i_csr_to_trap net46 net45 i_csr_ret_adr[31] i_csr_ret_adr[30] i_csr_ret_adr[29] i_csr_ret_adr[28]
+ i_csr_ret_adr[27] i_csr_ret_adr[26] i_csr_ret_adr[25] i_csr_ret_adr[24] i_csr_ret_adr[23] i_csr_ret_adr[22]
+ i_csr_ret_adr[21] i_csr_ret_adr[20] i_csr_ret_adr[19] i_csr_ret_adr[18] i_csr_ret_adr[17] i_csr_ret_adr[16]
+ i_csr_ret_adr[15] i_csr_ret_adr[14] i_csr_ret_adr[13] i_csr_ret_adr[12] i_csr_ret_adr[11] i_csr_ret_adr[10]
+ i_csr_ret_adr[9] i_csr_ret_adr[8] i_csr_ret_adr[7] i_csr_ret_adr[6] i_csr_ret_adr[5] i_csr_ret_adr[4]
+ i_csr_ret_adr[3] i_csr_ret_adr[2] i_csr_ret_adr[1] rv_alu1
x4 net53[31] net53[30] net53[29] net53[28] net53[27] net53[26] net53[25] net53[24] net53[23]
+ net53[22] net53[21] net53[20] net53[19] net53[18] net53[17] net53[16] net53[15] net53[14] net53[13] net53[12]
+ net53[11] net53[10] net53[9] net53[8] net53[7] net53[6] net53[5] net53[4] net53[3] net53[2] net53[1] net53[0]
+ clk_p[2] reset_n[1] net54[31] net54[30] net54[29] net54[28] net54[27] net54[26] net54[25] net54[24]
+ net54[23] net54[22] net54[21] net54[20] net54[19] net54[18] net54[17] net54[16] net54[15] net54[14] net54[13]
+ net54[12] net54[11] net54[10] net54[9] net54[8] net54[7] net54[6] net54[5] net54[4] net54[3] net54[2]
+ net54[1] net54[0] net41 net34 net2[4] net2[3] net2[2] net2[1] net2[0] net3[4] net3[3] net3[2] net3[1]
+ net3[0] net37[4] net37[3] net37[2] net37[1] net37[0] net55[31] net55[30] net55[29] net55[28] net55[27]
+ net55[26] net55[25] net55[24] net55[23] net55[22] net55[21] net55[20] net55[19] net55[18] net55[17] net55[16]
+ net55[15] net55[14] net55[13] net55[12] net55[11] net55[10] net55[9] net55[8] net55[7] net55[6] net55[5]
+ net55[4] net55[3] net55[2] net55[1] net55[0] rv_regs
x5 clk_p[0] o_reg_rdata1[31] o_reg_rdata1[30] o_reg_rdata1[29] o_reg_rdata1[28] o_reg_rdata1[27]
+ o_reg_rdata1[26] o_reg_rdata1[25] o_reg_rdata1[24] o_reg_rdata1[23] o_reg_rdata1[22] o_reg_rdata1[21]
+ o_reg_rdata1[20] o_reg_rdata1[19] o_reg_rdata1[18] o_reg_rdata1[17] o_reg_rdata1[16] o_reg_rdata1[15]
+ o_reg_rdata1[14] o_reg_rdata1[13] o_reg_rdata1[12] o_reg_rdata1[11] o_reg_rdata1[10] o_reg_rdata1[9] o_reg_rdata1[8]
+ o_reg_rdata1[7] o_reg_rdata1[6] o_reg_rdata1[5] o_reg_rdata1[4] o_reg_rdata1[3] o_reg_rdata1[2] o_reg_rdata1[1]
+ o_reg_rdata1[0] net32[4] net32[3] net32[2] net32[1] net32[0] net17[31] net17[30] net17[29] net17[28] net17[27]
+ net17[26] net17[25] net17[24] net17[23] net17[22] net17[21] net17[20] net17[19] net17[18] net17[17] net17[16]
+ net17[15] net17[14] net17[13] net17[12] net17[11] net17[10] net17[9] net17[8] net17[7] net17[6] net17[5]
+ net17[4] net17[3] net17[2] net17[1] net17[0] net31[4] net31[3] net31[2] net31[1] net31[0] net38[31]
+ net38[30] net38[29] net38[28] net38[27] net38[26] net38[25] net38[24] net38[23] net38[22] net38[21] net38[20]
+ net38[19] net38[18] net38[17] net38[16] net38[15] net38[14] net38[13] net38[12] net38[11] net38[10] net38[9]
+ net38[8] net38[7] net38[6] net38[5] net38[4] net38[3] net38[2] net38[1] net38[0] net33[4] net33[3] net33[2]
+ net33[1] net33[0] net55[31] net55[30] net55[29] net55[28] net55[27] net55[26] net55[25] net55[24] net55[23]
+ net55[22] net55[21] net55[20] net55[19] net55[18] net55[17] net55[16] net55[15] net55[14] net55[13] net55[12]
+ net55[11] net55[10] net55[9] net55[8] net55[7] net55[6] net55[5] net55[4] net55[3] net55[2] net55[1] net55[0]
+ net37[4] net37[3] net37[2] net37[1] net37[0] net44[31] net44[30] net44[29] net44[28] net44[27] net44[26]
+ net44[25] net44[24] net44[23] net44[22] net44[21] net44[20] net44[19] net44[18] net44[17] net44[16] net44[15]
+ net44[14] net44[13] net44[12] net44[11] net44[10] net44[9] net44[8] net44[7] net44[6] net44[5] net44[4]
+ net44[3] net44[2] net44[1] net44[0] net34 net36 net53[31] net53[30] net53[29] net53[28] net53[27] net53[26]
+ net53[25] net53[24] net53[23] net53[22] net53[21] net53[20] net53[19] net53[18] net53[17] net53[16] net53[15]
+ net53[14] net53[13] net53[12] net53[11] net53[10] net53[9] net53[8] net53[7] net53[6] net53[5] net53[4]
+ net53[3] net53[2] net53[1] net53[0] net54[31] net54[30] net54[29] net54[28] net54[27] net54[26] net54[25]
+ net54[24] net54[23] net54[22] net54[21] net54[20] net54[19] net54[18] net54[17] net54[16] net54[15] net54[14]
+ net54[13] net54[12] net54[11] net54[10] net54[9] net54[8] net54[7] net54[6] net54[5] net54[4] net54[3]
+ net54[2] net54[1] net54[0] net39[31] net39[30] net39[29] net39[28] net39[27] net39[26] net39[25] net39[24]
+ net39[23] net39[22] net39[21] net39[20] net39[19] net39[18] net39[17] net39[16] net39[15] net39[14] net39[13]
+ net39[12] net39[11] net39[10] net39[9] net39[8] net39[7] net39[6] net39[5] net39[4] net39[3] net39[2]
+ net39[1] net39[0] net40[31] net40[30] net40[29] net40[28] net40[27] net40[26] net40[25] net40[24] net40[23]
+ net40[22] net40[21] net40[20] net40[19] net40[18] net40[17] net40[16] net40[15] net40[14] net40[13] net40[12]
+ net40[11] net40[10] net40[9] net40[8] net40[7] net40[6] net40[5] net40[4] net40[3] net40[2] net40[1] net40[0]
+ rv_hazard
x6 alu2_pc_select clk_p[1] reset_n[0] net39[31] net39[30] net39[29] net39[28] net39[27] net39[26]
+ net39[25] net39[24] net39[23] net39[22] net39[21] net39[20] net39[19] net39[18] net39[17] net39[16] net39[15]
+ net39[14] net39[13] net39[12] net39[11] net39[10] net39[9] net39[8] net39[7] net39[6] net39[5] net39[4]
+ net39[3] net39[2] net39[1] net39[0] net18[31] net18[30] net18[29] net18[28] net18[27] net18[26] net18[25]
+ net18[24] net18[23] net18[22] net18[21] net18[20] net18[19] net18[18] net18[17] net18[16] net18[15] net18[14]
+ net18[13] net18[12] net18[11] net18[10] net18[9] net18[8] net18[7] net18[6] net18[5] net18[4] net18[3]
+ net18[2] net18[1] net18[0] o_data_adr[31] o_data_adr[30] o_data_adr[29] o_data_adr[28] o_data_adr[27]
+ o_data_adr[26] o_data_adr[25] o_data_adr[24] o_data_adr[23] o_data_adr[22] o_data_adr[21] o_data_adr[20]
+ o_data_adr[19] o_data_adr[18] o_data_adr[17] o_data_adr[16] o_data_adr[15] o_data_adr[14] o_data_adr[13]
+ o_data_adr[12] o_data_adr[11] o_data_adr[10] o_data_adr[9] o_data_adr[8] o_data_adr[7] o_data_adr[6] o_data_adr[5]
+ o_data_adr[4] o_data_adr[3] o_data_adr[2] o_data_adr[1] o_data_adr[0] o_data_write net19[31] net19[30] net19[29]
+ net19[28] net19[27] net19[26] net19[25] net19[24] net19[23] net19[22] net19[21] net19[20] net19[19] net19[18]
+ net19[17] net19[16] net19[15] net19[14] net19[13] net19[12] net19[11] net19[10] net19[9] net19[8] net19[7]
+ net19[6] net19[5] net19[4] net19[3] net19[2] net19[1] net19[0] net34 net20 net33[4] net33[3] net33[2]
+ net33[1] net33[0] net21 net22[4] net22[3] net22[2] net22[1] net22[0] alu2_pc_target[31] alu2_pc_target[30]
+ alu2_pc_target[29] alu2_pc_target[28] alu2_pc_target[27] alu2_pc_target[26] alu2_pc_target[25] alu2_pc_target[24]
+ alu2_pc_target[23] alu2_pc_target[22] alu2_pc_target[21] alu2_pc_target[20] alu2_pc_target[19] alu2_pc_target[18]
+ alu2_pc_target[17] alu2_pc_target[16] alu2_pc_target[15] alu2_pc_target[14] alu2_pc_target[13] alu2_pc_target[12]
+ alu2_pc_target[11] alu2_pc_target[10] alu2_pc_target[9] alu2_pc_target[8] alu2_pc_target[7] alu2_pc_target[6]
+ alu2_pc_target[5] alu2_pc_target[4] alu2_pc_target[3] alu2_pc_target[2] alu2_pc_target[1] alu2_res_src[2]
+ alu2_res_src[1] alu2_res_src[0] net23 net24 o_data_wdata[31] o_data_wdata[30] o_data_wdata[29] o_data_wdata[28]
+ o_data_wdata[27] o_data_wdata[26] o_data_wdata[25] o_data_wdata[24] o_data_wdata[23] o_data_wdata[22]
+ o_data_wdata[21] o_data_wdata[20] o_data_wdata[19] o_data_wdata[18] o_data_wdata[17] o_data_wdata[16]
+ o_data_wdata[15] o_data_wdata[14] o_data_wdata[13] o_data_wdata[12] o_data_wdata[11] o_data_wdata[10]
+ o_data_wdata[9] o_data_wdata[8] o_data_wdata[7] o_data_wdata[6] o_data_wdata[5] o_data_wdata[4] o_data_wdata[3]
+ o_data_wdata[2] o_data_wdata[1] o_data_wdata[0] o_data_sel[3] o_data_sel[2] o_data_sel[1] o_data_sel[0] net25[30]
+ net25[29] net25[28] net25[27] net25[26] net25[25] net25[24] net25[23] net25[22] net25[21] net25[20] net25[19]
+ net25[18] net25[17] net25[16] net25[15] net25[14] net25[13] net25[12] net25[11] net25[10] net25[9] net25[8]
+ net25[7] net25[6] net25[5] net25[4] net25[3] net25[2] net25[1] net25[0] net26[30] net26[29] net26[28]
+ net26[27] net26[26] net26[25] net26[24] net26[23] net26[22] net26[21] net26[20] net26[19] net26[18] net26[17]
+ net26[16] net26[15] net26[14] net26[13] net26[12] net26[11] net26[10] net26[9] net26[8] net26[7] net26[6]
+ net26[5] net26[4] net26[3] net26[2] net26[1] net26[0] net35[2] net35[1] net35[0] alu2_to_trap net27[30]
+ net27[29] net27[28] net27[27] net27[26] net27[25] net27[24] net27[23] net27[22] net27[21] net27[20] net27[19]
+ net27[18] net27[17] net27[16] net27[15] net27[14] net27[13] net27[12] net27[11] net27[10] net27[9] net27[8]
+ net27[7] net27[6] net27[5] net27[4] net27[3] net27[2] net27[1] net27[0] alu1_res_src[2] alu1_res_src[1]
+ alu1_res_src[0] net41 net28[2] net28[1] net28[0] net29[4] net29[3] net29[2] net29[1] net29[0] net30 net44[31]
+ net44[30] net44[29] net44[28] net44[27] net44[26] net44[25] net44[24] net44[23] net44[22] net44[21] net44[20]
+ net44[19] net44[18] net44[17] net44[16] net44[15] net44[14] net44[13] net44[12] net44[11] net44[10] net44[9]
+ net44[8] net44[7] net44[6] net44[5] net44[4] net44[3] net44[2] net44[1] net44[0] i_csr_read i_csr_data[31]
+ i_csr_data[30] i_csr_data[29] i_csr_data[28] i_csr_data[27] i_csr_data[26] i_csr_data[25] i_csr_data[24]
+ i_csr_data[23] i_csr_data[22] i_csr_data[21] i_csr_data[20] i_csr_data[19] i_csr_data[18] i_csr_data[17]
+ i_csr_data[16] i_csr_data[15] i_csr_data[14] i_csr_data[13] i_csr_data[12] i_csr_data[11] i_csr_data[10]
+ i_csr_data[9] i_csr_data[8] i_csr_data[7] i_csr_data[6] i_csr_data[5] i_csr_data[4] i_csr_data[3] i_csr_data[2]
+ i_csr_data[1] i_csr_data[0] net49 net51 rv_alu2
x7 clk_p[1] net36 net35[2] net35[1] net35[0] net40[31] net40[30] net40[29] net40[28] net40[27]
+ net40[26] net40[25] net40[24] net40[23] net40[22] net40[21] net40[20] net40[19] net40[18] net40[17] net40[16]
+ net40[15] net40[14] net40[13] net40[12] net40[11] net40[10] net40[9] net40[8] net40[7] net40[6] net40[5]
+ net40[4] net40[3] net40[2] net40[1] net40[0] net38[31] net38[30] net38[29] net38[28] net38[27] net38[26]
+ net38[25] net38[24] net38[23] net38[22] net38[21] net38[20] net38[19] net38[18] net38[17] net38[16] net38[15]
+ net38[14] net38[13] net38[12] net38[11] net38[10] net38[9] net38[8] net38[7] net38[6] net38[5] net38[4]
+ net38[3] net38[2] net38[1] net38[0] net37[4] net37[3] net37[2] net37[1] net37[0] net34 net33[4] net33[3]
+ net33[2] net33[1] net33[0] alu2_res_src[2] i_data_rdata[31] i_data_rdata[30] i_data_rdata[29]
+ i_data_rdata[28] i_data_rdata[27] i_data_rdata[26] i_data_rdata[25] i_data_rdata[24] i_data_rdata[23]
+ i_data_rdata[22] i_data_rdata[21] i_data_rdata[20] i_data_rdata[19] i_data_rdata[18] i_data_rdata[17]
+ i_data_rdata[16] i_data_rdata[15] i_data_rdata[14] i_data_rdata[13] i_data_rdata[12] i_data_rdata[11]
+ i_data_rdata[10] i_data_rdata[9] i_data_rdata[8] i_data_rdata[7] i_data_rdata[6] i_data_rdata[5] i_data_rdata[4]
+ i_data_rdata[3] i_data_rdata[2] i_data_rdata[1] i_data_rdata[0] net52 rv_write
x201 alu2_res_src[2] o_data_write VSS VSS VCC VCC o_data_req sky130_fd_sc_hd__or2_1
x202 o_data_req net34 VSS VSS VCC VCC o_instr_issued sky130_fd_sc_hd__or2_1
* noconn i_data_ack
x8 clk_p[2] net50 reset_n[1] net48 net47 fetch_pc_change net46 net42 net45 net41 alu1_res_src[2]
+ net49 net56 net57 net2[4] net2[3] net2[2] net2[1] net2[0] net3[4] net3[3] net3[2] net3[1] net3[0]
+ net22[4] net22[3] net22[2] net22[1] net22[0] net52 rv_ctrl
x203 net51 net24 net23 net43 VSS VSS VCC VCC net57 sky130_fd_sc_hd__o31a_1
* noconn #net56
x204 net48 net47 VSS VSS VCC VCC o_csr_masked sky130_fd_sc_hd__or2_1
**.ends
.end
